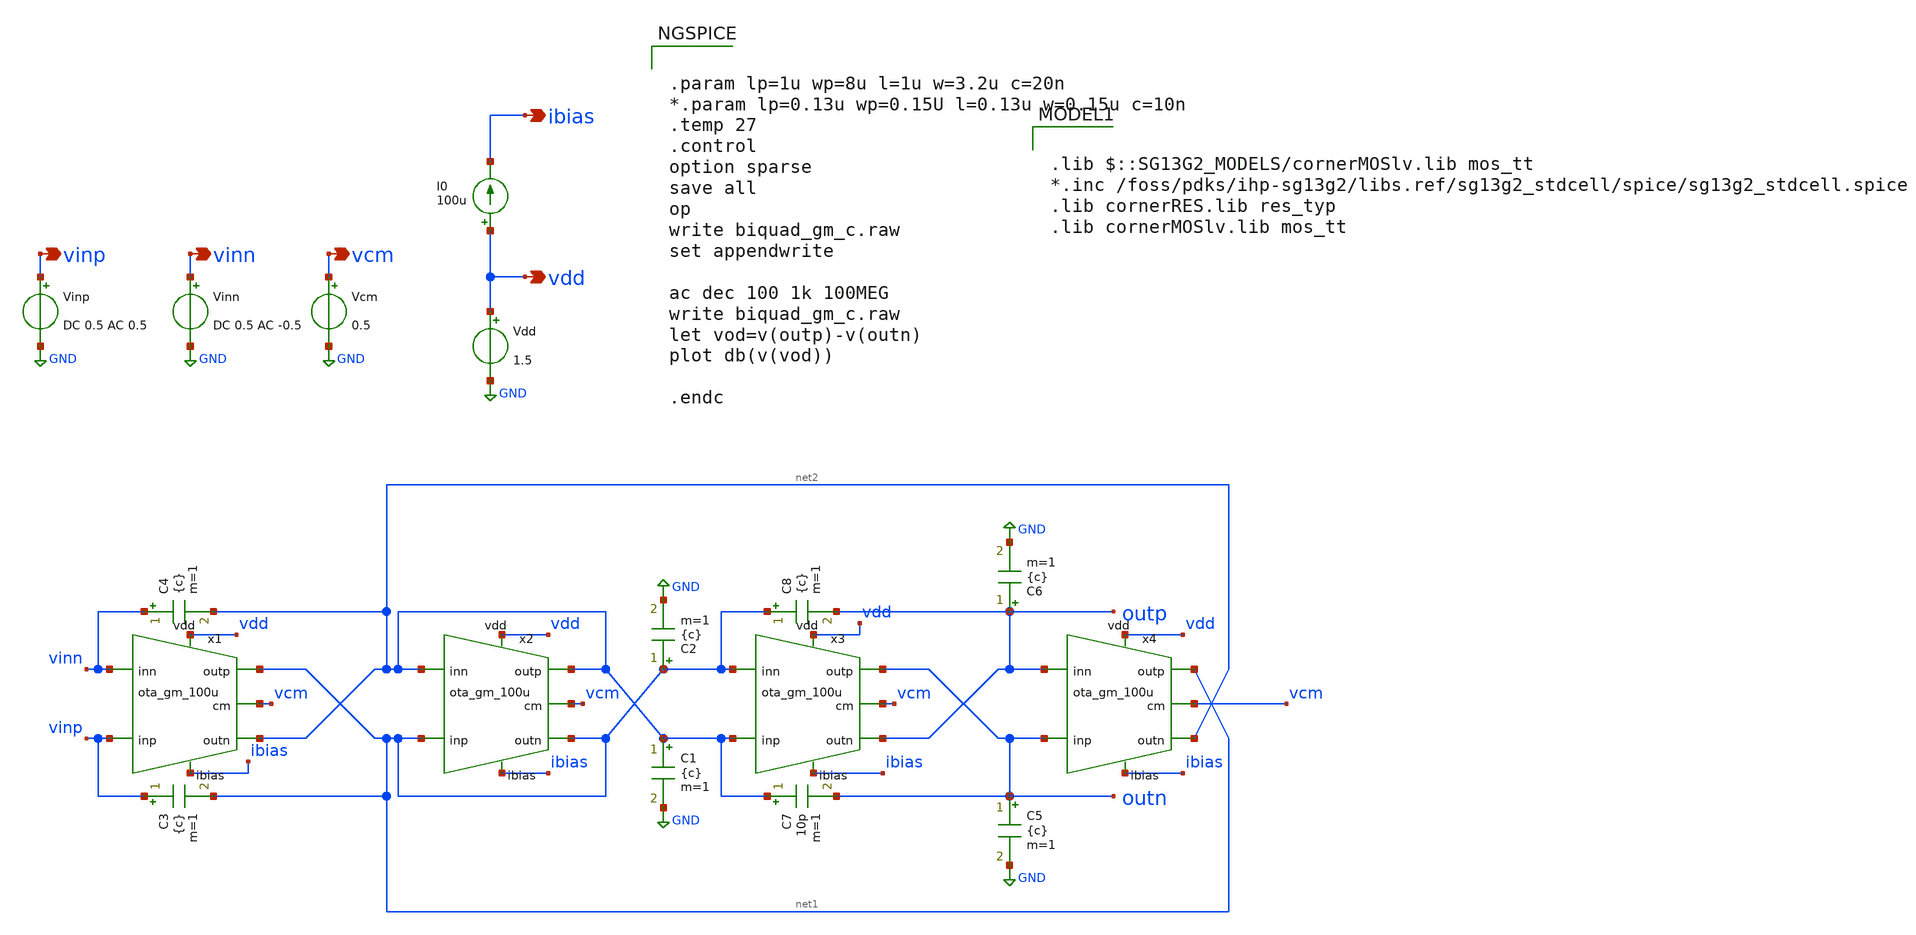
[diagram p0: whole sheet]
** sch_path: 2_Ideal_Cir/biquad_gm_c.sch
**.subckt biquad_gm_c vinp vinn vcm vdd ibias
*.opin vinp
*.opin vinn
*.opin vcm
*.opin vdd
*.opin ibias
x1 vinp vinn net1 net2 vcm vdd ibias ota_gm_100u
x2 net1 net2 net2 net1 vcm vdd ibias ota_gm_100u
C1 net2 GND {c} m=1
Vinp vinp GND DC 0.5 AC 0.5
Vinn vinn GND DC 0.5 AC -0.5
Vcm vcm GND 0.5
C2 net1 GND {c} m=1
C3 vinp net1 {c} m=1
C4 vinn net2 {c} m=1
x3 net2 net1 outn outp vcm vdd ibias ota_gm_100u
x4 outn outp net1 net2 vcm vdd ibias ota_gm_100u
C5 outn GND {c} m=1
C6 outp GND {c} m=1
C7 net2 outn 10p m=1
C8 net1 outp {c} m=1
Vdd vdd GND 1.5
I0 vdd ibias 100u
**** begin user architecture code


.param lp=1u wp=8u l=1u w=3.2u c=20n
*.param lp=0.13u wp=0.15U l=0.13u w=0.15u c=10n
.temp 27
.control
option sparse
save all
op
write biquad_gm_c.raw
set appendwrite

ac dec 100 1k 100MEG
write biquad_gm_c.raw
let vod=v(outp)-v(outn)
plot db(v(vod))

.endc



.lib $::SG13G2_MODELS/cornerMOSlv.lib mos_tt
*.inc /foss/pdks/ihp-sg13g2/libs.ref/sg13g2_stdcell/spice/sg13g2_stdcell.spice
.lib cornerRES.lib res_typ
.lib cornerMOSlv.lib mos_tt

**** end user architecture code
**.ends

* expanding   symbol:  2_Ideal_Cir/ota_gm_100u.sym # of pins=7
** sym_path: 3_Real_Cir/10_Real_Cir/ota_gm_100u.sym
** sch_path: 3_Real_Cir/10_Real_Cir/ota_gm_100u.sch
.subckt ota_gm_100u inp inn outp outn cm vdd ibias
*.ipin inp
*.ipin vdd
*.ipin inn
*.opin outp
*.ipin cm
*.ipin ibias
*.opin outn
XM1 net1 cm net2 GND sg13_lv_nmos w=0.15u l=0.13u ng=1 m=1 mm_ok=1
XM2 net1 net1 vdd vdd sg13_lv_pmos w=0.15u l=0.13u ng=1 m=1 mm_ok=1
XM3 net1 cm net2 GND sg13_lv_nmos w=0.15u l=0.13u ng=1 m=1 mm_ok=1
XM4 net1 net1 vdd vdd sg13_lv_pmos w=0.15u l=0.13u ng=1 m=1 mm_ok=1
XM5 outn net1 vdd vdd sg13_lv_pmos w=0.15u l=0.13u ng=1 m=1 mm_ok=1
XM6 outp net1 vdd vdd sg13_lv_pmos w=0.15u l=0.13u ng=1 m=1 mm_ok=1
XM7 outn inp net2 GND sg13_lv_nmos w=0.15u l=0.13u ng=1 m=1 mm_ok=1
XM8 outp inn net2 GND sg13_lv_nmos w=0.15u l=0.13u ng=1 m=1 mm_ok=1
XM9 ibias ibias net4 GND sg13_lv_nmos w=0.15u l=0.13u ng=1 m=1 mm_ok=1
XM11 net2 ibias net3 GND sg13_lv_nmos w=0.15u l=0.13u ng=1 m=1 mm_ok=1
XM10 net4 ibias GND GND sg13_lv_nmos w=0.15u l=0.13u ng=1 m=1 mm_ok=1
XM12 net3 ibias GND GND sg13_lv_nmos w=0.15u l=0.13u ng=1 m=1 mm_ok=1
.ends

.GLOBAL GND
.end
